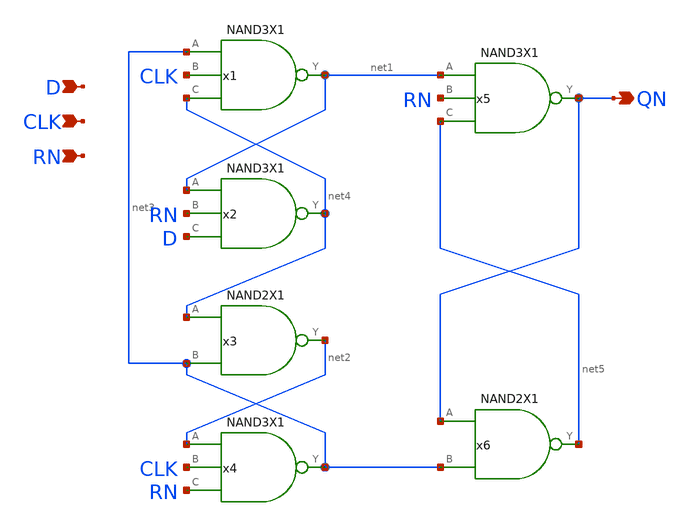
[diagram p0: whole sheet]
** sch_path: lib/xschem/DFFRNQNX1.sch
**.subckt DFFRNQNX1 QN D CLK RN
*.opin QN
*.ipin D
*.ipin CLK
*.ipin RN
x1 net1 net3 CLK net4 NAND3X1
x2 net4 net1 RN D NAND3X1
x3 net2 net4 net3 NAND2X1
x4 net3 net2 CLK RN NAND3X1
x5 QN net1 RN net5 NAND3X1
x6 net5 QN net3 NAND2X1
**.ends

* expanding   symbol:  NAND3X1.sym # of pins=4
** sym_path: lib/xschem/NAND3X1.sym
** sch_path: lib/xschem/NAND3X1.sch
.subckt NAND3X1 Y A B C
*.opin Y
*.ipin A
*.ipin B
*.ipin C
XM1 net2 A VSS VSS sky130_fd_pr__nfet_01v8 L=0.15 W=3 nf=1 ad='int((nf+1)/2) * W/nf * 0.29' as='int((nf+2)/2) * W/nf * 0.29'
+ pd='2*int((nf+1)/2) * (W/nf + 0.29)' ps='2*int((nf+2)/2) * (W/nf + 0.29)' nrd='0.29 / W' nrs='0.29 / W'
+ sa=0 sb=0 sd=0 mult=1 m=1
XM2 Y A VDD VDD sky130_fd_pr__pfet_01v8 L=0.15 W=nf=1 nf=1 ad='int((nf+1)/2) * W/nf * 0.29' as='int((nf+2)/2) * W/nf * 0.29'
+ pd='2*int((nf+1)/2) * (W/nf + 0.29)' ps='2*int((nf+2)/2) * (W/nf + 0.29)' nrd='0.29 / W' nrs='0.29 / W'
+ sa=0 sb=0 sd=0 mult=2 m=2
XM3 net1 B net2 VSS sky130_fd_pr__nfet_01v8 L=0.15 W=3 nf=1 ad='int((nf+1)/2) * W/nf * 0.29' as='int((nf+2)/2) * W/nf * 0.29'
+ pd='2*int((nf+1)/2) * (W/nf + 0.29)' ps='2*int((nf+2)/2) * (W/nf + 0.29)' nrd='0.29 / W' nrs='0.29 / W'
+ sa=0 sb=0 sd=0 mult=1 m=1
XM4 Y C net1 VSS sky130_fd_pr__nfet_01v8 L=0.15 W=3 nf=1 ad='int((nf+1)/2) * W/nf * 0.29' as='int((nf+2)/2) * W/nf * 0.29'
+ pd='2*int((nf+1)/2) * (W/nf + 0.29)' ps='2*int((nf+2)/2) * (W/nf + 0.29)' nrd='0.29 / W' nrs='0.29 / W'
+ sa=0 sb=0 sd=0 mult=1 m=1
XM5 Y B VDD VDD sky130_fd_pr__pfet_01v8 L=0.15 W=nf=1 nf=1 ad='int((nf+1)/2) * W/nf * 0.29' as='int((nf+2)/2) * W/nf * 0.29'
+ pd='2*int((nf+1)/2) * (W/nf + 0.29)' ps='2*int((nf+2)/2) * (W/nf + 0.29)' nrd='0.29 / W' nrs='0.29 / W'
+ sa=0 sb=0 sd=0 mult=2 m=2
XM6 Y C VDD VDD sky130_fd_pr__pfet_01v8 L=0.15 W=nf=1 nf=1 ad='int((nf+1)/2) * W/nf * 0.29' as='int((nf+2)/2) * W/nf * 0.29'
+ pd='2*int((nf+1)/2) * (W/nf + 0.29)' ps='2*int((nf+2)/2) * (W/nf + 0.29)' nrd='0.29 / W' nrs='0.29 / W'
+ sa=0 sb=0 sd=0 mult=2 m=2
.ends


* expanding   symbol:  NAND2X1.sym # of pins=3
** sym_path: lib/xschem/NAND2X1.sym
** sch_path: lib/xschem/NAND2X1.sch
.subckt NAND2X1 Y A B
*.ipin A
*.opin Y
*.ipin B
XM1 Y A VDD VDD sky130_fd_pr__pfet_01v8 L=0.15 W=2 nf=1 ad='int((nf+1)/2) * W/nf * 0.29' as='int((nf+2)/2) * W/nf * 0.29'
+ pd='2*int((nf+1)/2) * (W/nf + 0.29)' ps='2*int((nf+2)/2) * (W/nf + 0.29)' nrd='0.29 / W' nrs='0.29 / W'
+ sa=0 sb=0 sd=0 mult=1 m=1
XM5 Y A net1 VSS sky130_fd_pr__nfet_01v8 L=0.15 W=3 nf=1 ad='int((nf+1)/2) * W/nf * 0.29' as='int((nf+2)/2) * W/nf * 0.29'
+ pd='2*int((nf+1)/2) * (W/nf + 0.29)' ps='2*int((nf+2)/2) * (W/nf + 0.29)' nrd='0.29 / W' nrs='0.29 / W'
+ sa=0 sb=0 sd=0 mult=1 m=1
XM2 Y A VDD VDD sky130_fd_pr__pfet_01v8 L=0.15 W=2 nf=1 ad='int((nf+1)/2) * W/nf * 0.29' as='int((nf+2)/2) * W/nf * 0.29'
+ pd='2*int((nf+1)/2) * (W/nf + 0.29)' ps='2*int((nf+2)/2) * (W/nf + 0.29)' nrd='0.29 / W' nrs='0.29 / W'
+ sa=0 sb=0 sd=0 mult=1 m=1
XM3 Y B VDD VDD sky130_fd_pr__pfet_01v8 L=0.15 W=2 nf=1 ad='int((nf+1)/2) * W/nf * 0.29' as='int((nf+2)/2) * W/nf * 0.29'
+ pd='2*int((nf+1)/2) * (W/nf + 0.29)' ps='2*int((nf+2)/2) * (W/nf + 0.29)' nrd='0.29 / W' nrs='0.29 / W'
+ sa=0 sb=0 sd=0 mult=1 m=1
XM4 Y B VDD VDD sky130_fd_pr__pfet_01v8 L=0.15 W=2 nf=1 ad='int((nf+1)/2) * W/nf * 0.29' as='int((nf+2)/2) * W/nf * 0.29'
+ pd='2*int((nf+1)/2) * (W/nf + 0.29)' ps='2*int((nf+2)/2) * (W/nf + 0.29)' nrd='0.29 / W' nrs='0.29 / W'
+ sa=0 sb=0 sd=0 mult=1 m=1
XM6 net1 B VSS VSS sky130_fd_pr__nfet_01v8 L=0.15 W=3 nf=1 ad='int((nf+1)/2) * W/nf * 0.29' as='int((nf+2)/2) * W/nf * 0.29'
+ pd='2*int((nf+1)/2) * (W/nf + 0.29)' ps='2*int((nf+2)/2) * (W/nf + 0.29)' nrd='0.29 / W' nrs='0.29 / W'
+ sa=0 sb=0 sd=0 mult=1 m=1
.ends

.end
